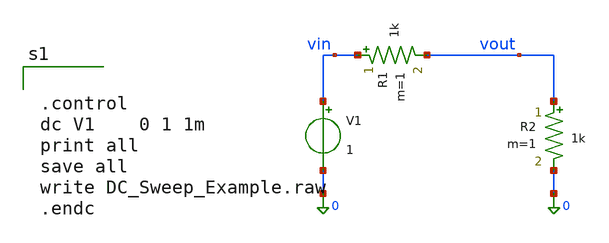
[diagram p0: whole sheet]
** sch_path: mag/layout/DC_Sweep_Example.sch
**.subckt DC_Sweep_Example
R1 vin vout 1k m=1
R2 vout 0 1k m=1
V1 vin 0 1
**** begin user architecture code


.control
dc V1    0 1 1m
print all
save all
write DC_Sweep_Example.raw
.endc

**** end user architecture code
**.ends
.end
